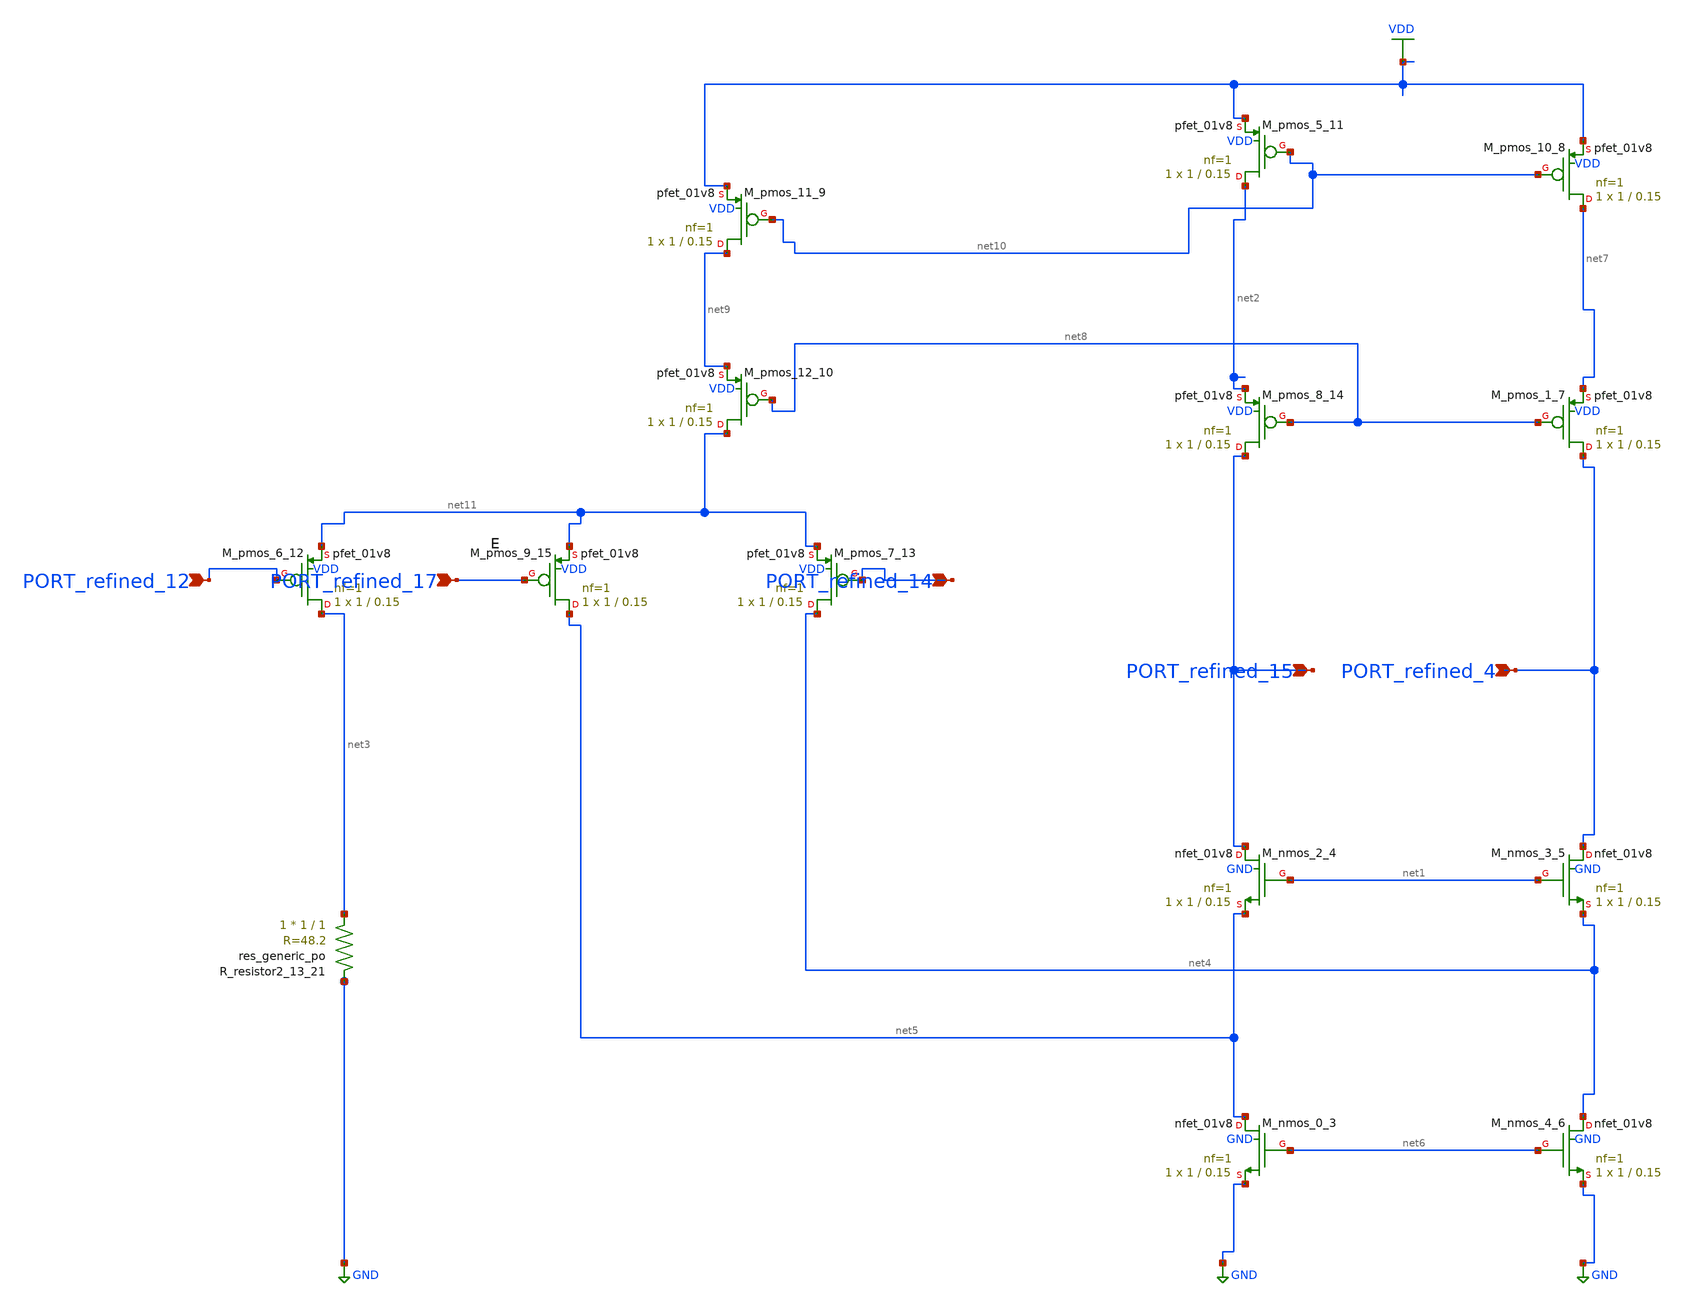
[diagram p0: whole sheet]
** sch_path: schematics/Image2Net/121.sch
**.subckt 121 PORT_refined_4 PORT_refined_12 PORT_refined_14 PORT_refined_15 PORT_refined_17
*.ipin PORT_refined_4
*.ipin PORT_refined_12
*.ipin PORT_refined_14
*.ipin PORT_refined_15
*.ipin PORT_refined_17
XM_nmos_0_3 net5 net6 GND GND sky130_fd_pr__nfet_01v8 L=0.15 W=1 nf=1 ad='int((1 + 1)/2) * 1 / 1 * 0.29'
+ as='int((1 + 2)/2) * 1 / 1 * 0.29' pd='2*int((1 + 1)/2) * (1 / 1 + 0.29)' ps='2*int((1 + 2)/2) * (1 / 1 + 0.29)'
+ nrd='0.29 / 1 ' nrs='0.29 / 1 ' sa=0 sb=0 sd=0 mult=1 m=1
XM_nmos_2_4 PORT_refined_15 net1 net5 GND sky130_fd_pr__nfet_01v8 L=0.15 W=1 nf=1 ad='int((1 + 1)/2) * 1 / 1 * 0.29'
+ as='int((1 + 2)/2) * 1 / 1 * 0.29' pd='2*int((1 + 1)/2) * (1 / 1 + 0.29)' ps='2*int((1 + 2)/2) * (1 / 1 + 0.29)'
+ nrd='0.29 / 1 ' nrs='0.29 / 1 ' sa=0 sb=0 sd=0 mult=1 m=1
XM_nmos_3_5 PORT_refined_4 net1 net4 GND sky130_fd_pr__nfet_01v8 L=0.15 W=1 nf=1 ad='int((1 + 1)/2) * 1 / 1 * 0.29'
+ as='int((1 + 2)/2) * 1 / 1 * 0.29' pd='2*int((1 + 1)/2) * (1 / 1 + 0.29)' ps='2*int((1 + 2)/2) * (1 / 1 + 0.29)'
+ nrd='0.29 / 1 ' nrs='0.29 / 1 ' sa=0 sb=0 sd=0 mult=1 m=1
XM_nmos_4_6 net4 net6 GND GND sky130_fd_pr__nfet_01v8 L=0.15 W=1 nf=1 ad='int((1 + 1)/2) * 1 / 1 * 0.29'
+ as='int((1 + 2)/2) * 1 / 1 * 0.29' pd='2*int((1 + 1)/2) * (1 / 1 + 0.29)' ps='2*int((1 + 2)/2) * (1 / 1 + 0.29)'
+ nrd='0.29 / 1 ' nrs='0.29 / 1 ' sa=0 sb=0 sd=0 mult=1 m=1
XM_pmos_1_7 PORT_refined_4 net8 net7 VDD sky130_fd_pr__pfet_01v8 L=0.15 W=1 nf=1 ad='int((1 + 1)/2) * 1 / 1 * 0.29'
+ as='int((1 + 2)/2) * 1 / 1 * 0.29' pd='2*int((1 + 1)/2) * (1 / 1 + 0.29)' ps='2*int((1 + 2)/2) * (1 / 1 + 0.29)'
+ nrd='0.29 / 1 ' nrs='0.29 / 1 ' sa=0 sb=0 sd=0 mult=1 m=1
XM_pmos_10_8 net7 net10 VDD VDD sky130_fd_pr__pfet_01v8 L=0.15 W=1 nf=1 ad='int((1 + 1)/2) * 1 / 1 * 0.29'
+ as='int((1 + 2)/2) * 1 / 1 * 0.29' pd='2*int((1 + 1)/2) * (1 / 1 + 0.29)' ps='2*int((1 + 2)/2) * (1 / 1 + 0.29)'
+ nrd='0.29 / 1 ' nrs='0.29 / 1 ' sa=0 sb=0 sd=0 mult=1 m=1
XM_pmos_11_9 net9 net10 VDD VDD sky130_fd_pr__pfet_01v8 L=0.15 W=1 nf=1 ad='int((1 + 1)/2) * 1 / 1 * 0.29'
+ as='int((1 + 2)/2) * 1 / 1 * 0.29' pd='2*int((1 + 1)/2) * (1 / 1 + 0.29)' ps='2*int((1 + 2)/2) * (1 / 1 + 0.29)'
+ nrd='0.29 / 1 ' nrs='0.29 / 1 ' sa=0 sb=0 sd=0 mult=1 m=1
XM_pmos_12_10 net11 net8 net9 VDD sky130_fd_pr__pfet_01v8 L=0.15 W=1 nf=1 ad='int((1 + 1)/2) * 1 / 1 * 0.29'
+ as='int((1 + 2)/2) * 1 / 1 * 0.29' pd='2*int((1 + 1)/2) * (1 / 1 + 0.29)' ps='2*int((1 + 2)/2) * (1 / 1 + 0.29)'
+ nrd='0.29 / 1 ' nrs='0.29 / 1 ' sa=0 sb=0 sd=0 mult=1 m=1
XM_pmos_5_11 net2 net10 VDD VDD sky130_fd_pr__pfet_01v8 L=0.15 W=1 nf=1 ad='int((1 + 1)/2) * 1 / 1 * 0.29'
+ as='int((1 + 2)/2) * 1 / 1 * 0.29' pd='2*int((1 + 1)/2) * (1 / 1 + 0.29)' ps='2*int((1 + 2)/2) * (1 / 1 + 0.29)'
+ nrd='0.29 / 1 ' nrs='0.29 / 1 ' sa=0 sb=0 sd=0 mult=1 m=1
XM_pmos_6_12 net3 PORT_refined_12 net11 VDD sky130_fd_pr__pfet_01v8 L=0.15 W=1 nf=1 ad='int((1 + 1)/2) * 1 / 1 * 0.29'
+ as='int((1 + 2)/2) * 1 / 1 * 0.29' pd='2*int((1 + 1)/2) * (1 / 1 + 0.29)' ps='2*int((1 + 2)/2) * (1 / 1 + 0.29)'
+ nrd='0.29 / 1 ' nrs='0.29 / 1 ' sa=0 sb=0 sd=0 mult=1 m=1
XM_pmos_7_13 net4 PORT_refined_14 net11 VDD sky130_fd_pr__pfet_01v8 L=0.15 W=1 nf=1 ad='int((1 + 1)/2) * 1 / 1 * 0.29'
+ as='int((1 + 2)/2) * 1 / 1 * 0.29' pd='2*int((1 + 1)/2) * (1 / 1 + 0.29)' ps='2*int((1 + 2)/2) * (1 / 1 + 0.29)'
+ nrd='0.29 / 1 ' nrs='0.29 / 1 ' sa=0 sb=0 sd=0 mult=1 m=1
XM_pmos_8_14 PORT_refined_15 net8 net2 VDD sky130_fd_pr__pfet_01v8 L=0.15 W=1 nf=1 ad='int((1 + 1)/2) * 1 / 1 * 0.29'
+ as='int((1 + 2)/2) * 1 / 1 * 0.29' pd='2*int((1 + 1)/2) * (1 / 1 + 0.29)' ps='2*int((1 + 2)/2) * (1 / 1 + 0.29)'
+ nrd='0.29 / 1 ' nrs='0.29 / 1 ' sa=0 sb=0 sd=0 mult=1 m=1
XM_pmos_9_15 net5 PORT_refined_17 net11 VDD sky130_fd_pr__pfet_01v8 L=0.15 W=1 nf=1 ad='int((1 + 1)/2) * 1 / 1 * 0.29'
+ as='int((1 + 2)/2) * 1 / 1 * 0.29' pd='2*int((1 + 1)/2) * (1 / 1 + 0.29)' ps='2*int((1 + 2)/2) * (1 / 1 + 0.29)'
+ nrd='0.29 / 1 ' nrs='0.29 / 1 ' sa=0 sb=0 sd=0 mult=1 m=1
XR_resistor2_13_21 net3 GND sky130_fd_pr__res_generic_po W=1 L=1 m=1
**.ends
.GLOBAL GND
.GLOBAL VDD
.end
